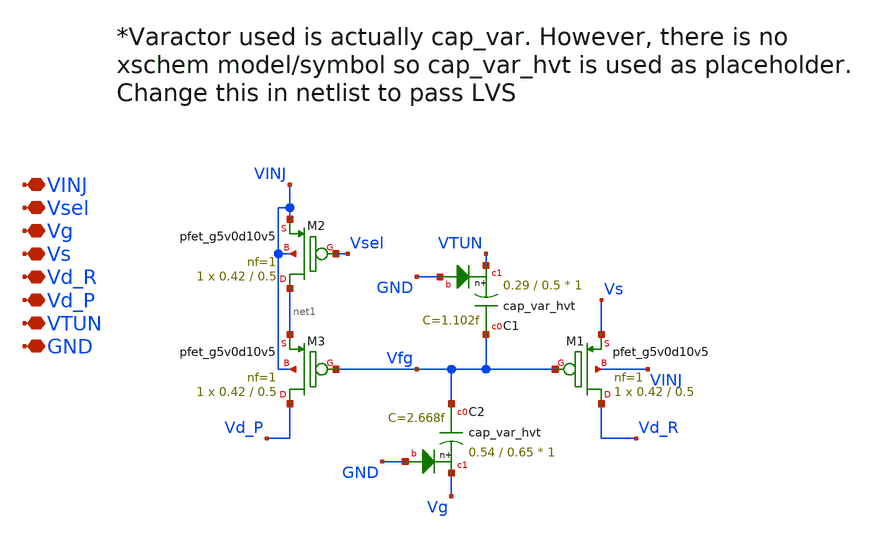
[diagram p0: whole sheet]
** sch_path: sky130_cells/Floating_Gates/Indirect/FG_Indirect.sch
**.subckt FG_Indirect VINJ Vsel Vg Vs Vd_R Vd_P VTUN GND
*.iopin VINJ
*.iopin Vsel
*.iopin Vg
*.iopin Vs
*.iopin Vd_R
*.iopin Vd_P
*.iopin VTUN
*.iopin GND
XM1 Vd_R Vfg Vs VINJ sky130_fd_pr__pfet_g5v0d10v5 L=0.5 W=0.42 nf=1 ad='int((nf+1)/2) * W/nf * 0.29'
+ as='int((nf+2)/2) * W/nf * 0.29' pd='2*int((nf+1)/2) * (W/nf + 0.29)' ps='2*int((nf+2)/2) * (W/nf + 0.29)'
+ nrd='0.29 / W' nrs='0.29 / W' sa=0 sb=0 sd=0 mult=1 m=1
XM2 net1 Vsel VINJ VINJ sky130_fd_pr__pfet_g5v0d10v5 L=0.5 W=0.42 nf=1 ad='int((nf+1)/2) * W/nf * 0.29'
+ as='int((nf+2)/2) * W/nf * 0.29' pd='2*int((nf+1)/2) * (W/nf + 0.29)' ps='2*int((nf+2)/2) * (W/nf + 0.29)'
+ nrd='0.29 / W' nrs='0.29 / W' sa=0 sb=0 sd=0 mult=1 m=1
XM3 Vd_P Vfg net1 VINJ sky130_fd_pr__pfet_g5v0d10v5 L=0.5 W=0.42 nf=1 ad='int((nf+1)/2) * W/nf * 0.29'
+ as='int((nf+2)/2) * W/nf * 0.29' pd='2*int((nf+1)/2) * (W/nf + 0.29)' ps='2*int((nf+2)/2) * (W/nf + 0.29)'
+ nrd='0.29 / W' nrs='0.29 / W' sa=0 sb=0 sd=0 mult=1 m=1
XC1 Vfg VTUN GND sky130_fd_pr__cap_var_hvt W=0.29 L=0.5 VM=1 m=1
XC2 Vfg Vg GND sky130_fd_pr__cap_var_hvt W=0.54 L=0.65 VM=1 m=1
**.ends
.end
